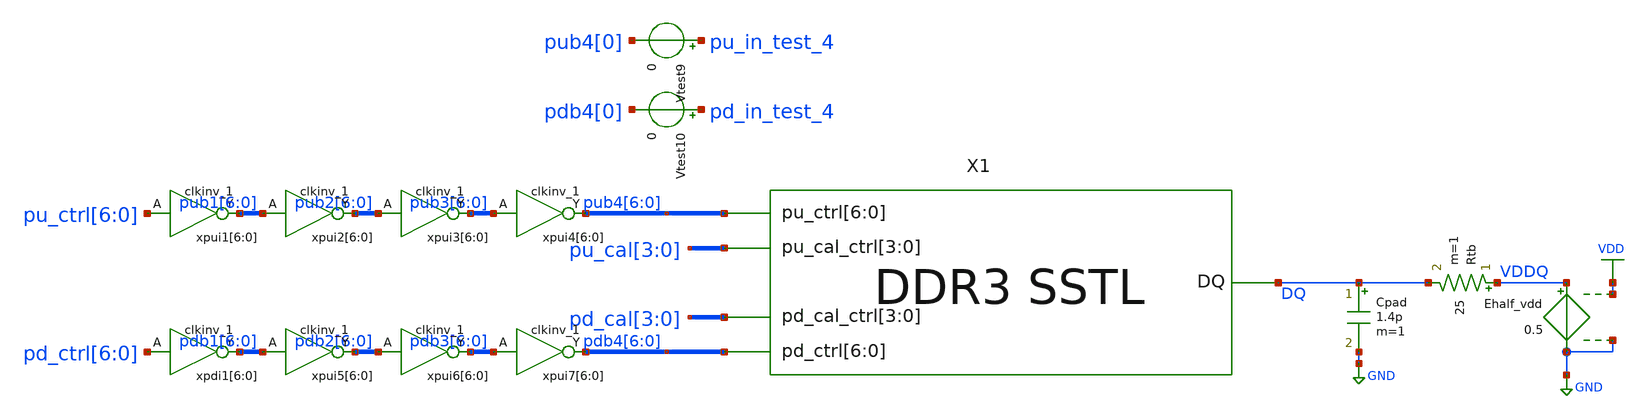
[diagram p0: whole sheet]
** sch_path: schem/sstl_slew_tb.sch
* Copyright 2021 Stefan Frederik Schippers
* Licensed under the Apache License, Version 2.0 (the "License");
* you may not use this file except in compliance with the License.
* You may obtain a copy of the License at
* https://www.apache.org/licenses/LICENSE-2.0
* Unless required by applicable law or agreed to in writing, software
* distributed under the License is distributed on an "AS IS" BASIS,
* WITHOUT WARRANTIES OR CONDITIONS OF ANY KIND, either express or implied.
* See the License for the specific language governing permissions and
* limitations under the License.
**.subckt sstl_slew_tb
X1 DQ pdb4[6] pdb4[5] pdb4[4] pdb4[3] pdb4[2] pdb4[1] pdb4[0] pub4[6] pub4[5] pub4[4] pub4[3]
+ pub4[2] pub4[1] pub4[0] pd_cal[3] pd_cal[2] pd_cal[1] pd_cal[0] pu_cal[3] pu_cal[2] pu_cal[1] pu_cal[0]
+ SSTL
Rtb VDDQ DQ 25 m=1
Cpad DQ GND 1.4p m=1
Ehalf_vdd VDDQ GND VDD GND 0.5
xpui1[6] pu_ctrl[6] GND GND VDD VDD pub1[6] sky130_fd_sc_hd__clkinv_1
xpui1[5] pu_ctrl[5] GND GND VDD VDD pub1[5] sky130_fd_sc_hd__clkinv_1
xpui1[4] pu_ctrl[4] GND GND VDD VDD pub1[4] sky130_fd_sc_hd__clkinv_1
xpui1[3] pu_ctrl[3] GND GND VDD VDD pub1[3] sky130_fd_sc_hd__clkinv_1
xpui1[2] pu_ctrl[2] GND GND VDD VDD pub1[2] sky130_fd_sc_hd__clkinv_1
xpui1[1] pu_ctrl[1] GND GND VDD VDD pub1[1] sky130_fd_sc_hd__clkinv_1
xpui1[0] pu_ctrl[0] GND GND VDD VDD pub1[0] sky130_fd_sc_hd__clkinv_1
xpdi1[6] pd_ctrl[6] VGND VNB VPB VPWR pdb1[6] sky130_fd_sc_hd__clkinv_1
xpdi1[5] pd_ctrl[5] VGND VNB VPB VPWR pdb1[5] sky130_fd_sc_hd__clkinv_1
xpdi1[4] pd_ctrl[4] VGND VNB VPB VPWR pdb1[4] sky130_fd_sc_hd__clkinv_1
xpdi1[3] pd_ctrl[3] VGND VNB VPB VPWR pdb1[3] sky130_fd_sc_hd__clkinv_1
xpdi1[2] pd_ctrl[2] VGND VNB VPB VPWR pdb1[2] sky130_fd_sc_hd__clkinv_1
xpdi1[1] pd_ctrl[1] VGND VNB VPB VPWR pdb1[1] sky130_fd_sc_hd__clkinv_1
xpdi1[0] pd_ctrl[0] VGND VNB VPB VPWR pdb1[0] sky130_fd_sc_hd__clkinv_1
Vtest9 pu_in_test_4 pub4[0] 0
Vtest10 pd_in_test_4 pdb4[0] 0
xpui2[6] pub1[6] GND GND VDD VDD pub2[6] sky130_fd_sc_hd__clkinv_1
xpui2[5] pub1[5] GND GND VDD VDD pub2[5] sky130_fd_sc_hd__clkinv_1
xpui2[4] pub1[4] GND GND VDD VDD pub2[4] sky130_fd_sc_hd__clkinv_1
xpui2[3] pub1[3] GND GND VDD VDD pub2[3] sky130_fd_sc_hd__clkinv_1
xpui2[2] pub1[2] GND GND VDD VDD pub2[2] sky130_fd_sc_hd__clkinv_1
xpui2[1] pub1[1] GND GND VDD VDD pub2[1] sky130_fd_sc_hd__clkinv_1
xpui2[0] pub1[0] GND GND VDD VDD pub2[0] sky130_fd_sc_hd__clkinv_1
xpui3[6] pub2[6] GND GND VDD VDD pub3[6] sky130_fd_sc_hd__clkinv_1
xpui3[5] pub2[5] GND GND VDD VDD pub3[5] sky130_fd_sc_hd__clkinv_1
xpui3[4] pub2[4] GND GND VDD VDD pub3[4] sky130_fd_sc_hd__clkinv_1
xpui3[3] pub2[3] GND GND VDD VDD pub3[3] sky130_fd_sc_hd__clkinv_1
xpui3[2] pub2[2] GND GND VDD VDD pub3[2] sky130_fd_sc_hd__clkinv_1
xpui3[1] pub2[1] GND GND VDD VDD pub3[1] sky130_fd_sc_hd__clkinv_1
xpui3[0] pub2[0] GND GND VDD VDD pub3[0] sky130_fd_sc_hd__clkinv_1
xpui4[6] pub3[6] GND GND VDD VDD pub4[6] sky130_fd_sc_hd__clkinv_1
xpui4[5] pub3[5] GND GND VDD VDD pub4[5] sky130_fd_sc_hd__clkinv_1
xpui4[4] pub3[4] GND GND VDD VDD pub4[4] sky130_fd_sc_hd__clkinv_1
xpui4[3] pub3[3] GND GND VDD VDD pub4[3] sky130_fd_sc_hd__clkinv_1
xpui4[2] pub3[2] GND GND VDD VDD pub4[2] sky130_fd_sc_hd__clkinv_1
xpui4[1] pub3[1] GND GND VDD VDD pub4[1] sky130_fd_sc_hd__clkinv_1
xpui4[0] pub3[0] GND GND VDD VDD pub4[0] sky130_fd_sc_hd__clkinv_1
xpui5[6] pdb1[6] GND GND VDD VDD pdb2[6] sky130_fd_sc_hd__clkinv_1
xpui5[5] pdb1[5] GND GND VDD VDD pdb2[5] sky130_fd_sc_hd__clkinv_1
xpui5[4] pdb1[4] GND GND VDD VDD pdb2[4] sky130_fd_sc_hd__clkinv_1
xpui5[3] pdb1[3] GND GND VDD VDD pdb2[3] sky130_fd_sc_hd__clkinv_1
xpui5[2] pdb1[2] GND GND VDD VDD pdb2[2] sky130_fd_sc_hd__clkinv_1
xpui5[1] pdb1[1] GND GND VDD VDD pdb2[1] sky130_fd_sc_hd__clkinv_1
xpui5[0] pdb1[0] GND GND VDD VDD pdb2[0] sky130_fd_sc_hd__clkinv_1
xpui6[6] pdb2[6] GND GND VDD VDD pdb3[6] sky130_fd_sc_hd__clkinv_1
xpui6[5] pdb2[5] GND GND VDD VDD pdb3[5] sky130_fd_sc_hd__clkinv_1
xpui6[4] pdb2[4] GND GND VDD VDD pdb3[4] sky130_fd_sc_hd__clkinv_1
xpui6[3] pdb2[3] GND GND VDD VDD pdb3[3] sky130_fd_sc_hd__clkinv_1
xpui6[2] pdb2[2] GND GND VDD VDD pdb3[2] sky130_fd_sc_hd__clkinv_1
xpui6[1] pdb2[1] GND GND VDD VDD pdb3[1] sky130_fd_sc_hd__clkinv_1
xpui6[0] pdb2[0] GND GND VDD VDD pdb3[0] sky130_fd_sc_hd__clkinv_1
xpui7[6] pdb3[6] GND GND VDD VDD pdb4[6] sky130_fd_sc_hd__clkinv_1
xpui7[5] pdb3[5] GND GND VDD VDD pdb4[5] sky130_fd_sc_hd__clkinv_1
xpui7[4] pdb3[4] GND GND VDD VDD pdb4[4] sky130_fd_sc_hd__clkinv_1
xpui7[3] pdb3[3] GND GND VDD VDD pdb4[3] sky130_fd_sc_hd__clkinv_1
xpui7[2] pdb3[2] GND GND VDD VDD pdb4[2] sky130_fd_sc_hd__clkinv_1
xpui7[1] pdb3[1] GND GND VDD VDD pdb4[1] sky130_fd_sc_hd__clkinv_1
xpui7[0] pdb3[0] GND GND VDD VDD pdb4[0] sky130_fd_sc_hd__clkinv_1
**** begin user architecture code
 ** Local library links to pdk
.lib ./sky130/libs/SED_process_SED_lib.spice SED_process_SED
.include $::SKYWATER_STDCELLS/sky130_fd_sc_hd.spice

**** end user architecture code
**.ends

* expanding   symbol:  SSTL.sym # of pins=5
** sym_path: schem/SSTL.sym
** sch_path: schem/SSTL.sch
.subckt SSTL DQ pd_ctrl[6] pd_ctrl[5] pd_ctrl[4] pd_ctrl[3] pd_ctrl[2] pd_ctrl[1] pd_ctrl[0]
+ pu_ctrl[6] pu_ctrl[5] pu_ctrl[4] pu_ctrl[3] pu_ctrl[2] pu_ctrl[1] pu_ctrl[0] pd_cal_ctrl[3] pd_cal_ctrl[2]
+ pd_cal_ctrl[1] pd_cal_ctrl[0] pu_cal_ctrl[3] pu_cal_ctrl[2] pu_cal_ctrl[1] pu_cal_ctrl[0]
*.iopin DQ
*.ipin pu_cal_ctrl[3],pu_cal_ctrl[2],pu_cal_ctrl[1],pu_cal_ctrl[0]
*.ipin pd_cal_ctrl[3],pd_cal_ctrl[2],pd_cal_ctrl[1],pd_cal_ctrl[0]
*.ipin pu_ctrl[6],pu_ctrl[5],pu_ctrl[4],pu_ctrl[3],pu_ctrl[2],pu_ctrl[1],pu_ctrl[0]
*.ipin pd_ctrl[6],pd_ctrl[5],pd_ctrl[4],pd_ctrl[3],pd_ctrl[2],pd_ctrl[1],pd_ctrl[0]
X1 DQ n_pu_ctrl[6] n_pu_cal_ctrl[3] n_pu_cal_ctrl[2] n_pu_cal_ctrl[1] n_pu_cal_ctrl[0] p-leg
X2 DQ pd_ctrl_buff[6] pd_cal_ctrl[3] pd_cal_ctrl[2] pd_cal_ctrl[1] pd_cal_ctrl[0] n-leg
X3 DQ n_pu_ctrl[5] n_pu_cal_ctrl[3] n_pu_cal_ctrl[2] n_pu_cal_ctrl[1] n_pu_cal_ctrl[0] p-leg
X4 DQ pd_ctrl_buff[5] pd_cal_ctrl[3] pd_cal_ctrl[2] pd_cal_ctrl[1] pd_cal_ctrl[0] n-leg
X5 DQ n_pu_ctrl[4] n_pu_cal_ctrl[3] n_pu_cal_ctrl[2] n_pu_cal_ctrl[1] n_pu_cal_ctrl[0] p-leg
X6 DQ pd_ctrl_buff[4] pd_cal_ctrl[3] pd_cal_ctrl[2] pd_cal_ctrl[1] pd_cal_ctrl[0] n-leg
X7 DQ n_pu_ctrl[3] n_pu_cal_ctrl[3] n_pu_cal_ctrl[2] n_pu_cal_ctrl[1] n_pu_cal_ctrl[0] p-leg
X8 DQ pd_ctrl_buff[3] pd_cal_ctrl[3] pd_cal_ctrl[2] pd_cal_ctrl[1] pd_cal_ctrl[0] n-leg
X9 DQ n_pu_ctrl[2] n_pu_cal_ctrl[3] n_pu_cal_ctrl[2] n_pu_cal_ctrl[1] n_pu_cal_ctrl[0] p-leg
X10 DQ pd_ctrl_buff[2] pd_cal_ctrl[3] pd_cal_ctrl[2] pd_cal_ctrl[1] pd_cal_ctrl[0] n-leg
X11 DQ n_pu_ctrl[1] n_pu_cal_ctrl[3] n_pu_cal_ctrl[2] n_pu_cal_ctrl[1] n_pu_cal_ctrl[0] p-leg
X12 DQ pd_ctrl_buff[1] pd_cal_ctrl[3] pd_cal_ctrl[2] pd_cal_ctrl[1] pd_cal_ctrl[0] n-leg
X13 DQ n_pu_ctrl[0] n_pu_cal_ctrl[3] n_pu_cal_ctrl[2] n_pu_cal_ctrl[1] n_pu_cal_ctrl[0] p-leg
X14 DQ pd_ctrl_buff[0] pd_cal_ctrl[3] pd_cal_ctrl[2] pd_cal_ctrl[1] pd_cal_ctrl[0] n-leg
xpd_buff_4[6] pdc2[6] VGND VNB VPB VPWR pdc4[6] sky130_fd_sc_hd__clkinv_4
xpd_buff_4[5] pdc2[5] VGND VNB VPB VPWR pdc4[5] sky130_fd_sc_hd__clkinv_4
xpd_buff_4[4] pdc2[4] VGND VNB VPB VPWR pdc4[4] sky130_fd_sc_hd__clkinv_4
xpd_buff_4[3] pdc2[3] VGND VNB VPB VPWR pdc4[3] sky130_fd_sc_hd__clkinv_4
xpd_buff_4[2] pdc2[2] VGND VNB VPB VPWR pdc4[2] sky130_fd_sc_hd__clkinv_4
xpd_buff_4[1] pdc2[1] VGND VNB VPB VPWR pdc4[1] sky130_fd_sc_hd__clkinv_4
xpd_buff_4[0] pdc2[0] VGND VNB VPB VPWR pdc4[0] sky130_fd_sc_hd__clkinv_4
xpd_buff_6[6] pdc4[6] VGND VNB VPB VPWR pd_ctrl_buff[6] sky130_fd_sc_hd__clkbuf_8
xpd_buff_6[5] pdc4[5] VGND VNB VPB VPWR pd_ctrl_buff[5] sky130_fd_sc_hd__clkbuf_8
xpd_buff_6[4] pdc4[4] VGND VNB VPB VPWR pd_ctrl_buff[4] sky130_fd_sc_hd__clkbuf_8
xpd_buff_6[3] pdc4[3] VGND VNB VPB VPWR pd_ctrl_buff[3] sky130_fd_sc_hd__clkbuf_8
xpd_buff_6[2] pdc4[2] VGND VNB VPB VPWR pd_ctrl_buff[2] sky130_fd_sc_hd__clkbuf_8
xpd_buff_6[1] pdc4[1] VGND VNB VPB VPWR pd_ctrl_buff[1] sky130_fd_sc_hd__clkbuf_8
xpd_buff_6[0] pdc4[0] VGND VNB VPB VPWR pd_ctrl_buff[0] sky130_fd_sc_hd__clkbuf_8
xpu_buff_4[6] pu_ctrl[6] VGND VNB VPB VPWR puc4[6] sky130_fd_sc_hd__clkbuf_16
xpu_buff_4[5] pu_ctrl[5] VGND VNB VPB VPWR puc4[5] sky130_fd_sc_hd__clkbuf_16
xpu_buff_4[4] pu_ctrl[4] VGND VNB VPB VPWR puc4[4] sky130_fd_sc_hd__clkbuf_16
xpu_buff_4[3] pu_ctrl[3] VGND VNB VPB VPWR puc4[3] sky130_fd_sc_hd__clkbuf_16
xpu_buff_4[2] pu_ctrl[2] VGND VNB VPB VPWR puc4[2] sky130_fd_sc_hd__clkbuf_16
xpu_buff_4[1] pu_ctrl[1] VGND VNB VPB VPWR puc4[1] sky130_fd_sc_hd__clkbuf_16
xpu_buff_4[0] pu_ctrl[0] VGND VNB VPB VPWR puc4[0] sky130_fd_sc_hd__clkbuf_16
xpu_buff_6[6] puc4[6] VGND VNB VPB VPWR n_pu_ctrl[6] sky130_fd_sc_hd__clkinv_16
xpu_buff_6[5] puc4[5] VGND VNB VPB VPWR n_pu_ctrl[5] sky130_fd_sc_hd__clkinv_16
xpu_buff_6[4] puc4[4] VGND VNB VPB VPWR n_pu_ctrl[4] sky130_fd_sc_hd__clkinv_16
xpu_buff_6[3] puc4[3] VGND VNB VPB VPWR n_pu_ctrl[3] sky130_fd_sc_hd__clkinv_16
xpu_buff_6[2] puc4[2] VGND VNB VPB VPWR n_pu_ctrl[2] sky130_fd_sc_hd__clkinv_16
xpu_buff_6[1] puc4[1] VGND VNB VPB VPWR n_pu_ctrl[1] sky130_fd_sc_hd__clkinv_16
xpu_buff_6[0] puc4[0] VGND VNB VPB VPWR n_pu_ctrl[0] sky130_fd_sc_hd__clkinv_16
xpu_cal_inv[3] pu_cal_ctrl[3] VGND VNB VPB VPWR n_pu_cal_ctrl[3] sky130_fd_sc_hd__inv_1
xpu_cal_inv[2] pu_cal_ctrl[2] VGND VNB VPB VPWR n_pu_cal_ctrl[2] sky130_fd_sc_hd__inv_1
xpu_cal_inv[1] pu_cal_ctrl[1] VGND VNB VPB VPWR n_pu_cal_ctrl[1] sky130_fd_sc_hd__inv_1
xpu_cal_inv[0] pu_cal_ctrl[0] VGND VNB VPB VPWR n_pu_cal_ctrl[0] sky130_fd_sc_hd__inv_1
V1 VDD VPWR 0
V2 VGND GND 0
V3 VDD VPB 0
V4 VNB GND 0
Vpd_ctrl_0 v_pd_ctrl_0 pd_ctrl_buff[6] 0
Vpd_ctrl_1 v_pu_ctrl_0 n_pu_ctrl[6] 0
xpu_buff_2[6] puc4[6] VGND VNB VPB VPWR n_pu_ctrl[6] sky130_fd_sc_hd__clkinv_16
xpu_buff_2[5] puc4[5] VGND VNB VPB VPWR n_pu_ctrl[5] sky130_fd_sc_hd__clkinv_16
xpu_buff_2[4] puc4[4] VGND VNB VPB VPWR n_pu_ctrl[4] sky130_fd_sc_hd__clkinv_16
xpu_buff_2[3] puc4[3] VGND VNB VPB VPWR n_pu_ctrl[3] sky130_fd_sc_hd__clkinv_16
xpu_buff_2[2] puc4[2] VGND VNB VPB VPWR n_pu_ctrl[2] sky130_fd_sc_hd__clkinv_16
xpu_buff_2[1] puc4[1] VGND VNB VPB VPWR n_pu_ctrl[1] sky130_fd_sc_hd__clkinv_16
xpu_buff_2[0] puc4[0] VGND VNB VPB VPWR n_pu_ctrl[0] sky130_fd_sc_hd__clkinv_16
xpd_buff_1[6] pd_ctrl[6] VGND VNB VPB VPWR pdc2[6] sky130_fd_sc_hd__clkinv_4
xpd_buff_1[5] pd_ctrl[5] VGND VNB VPB VPWR pdc2[5] sky130_fd_sc_hd__clkinv_4
xpd_buff_1[4] pd_ctrl[4] VGND VNB VPB VPWR pdc2[4] sky130_fd_sc_hd__clkinv_4
xpd_buff_1[3] pd_ctrl[3] VGND VNB VPB VPWR pdc2[3] sky130_fd_sc_hd__clkinv_4
xpd_buff_1[2] pd_ctrl[2] VGND VNB VPB VPWR pdc2[2] sky130_fd_sc_hd__clkinv_4
xpd_buff_1[1] pd_ctrl[1] VGND VNB VPB VPWR pdc2[1] sky130_fd_sc_hd__clkinv_4
xpd_buff_1[0] pd_ctrl[0] VGND VNB VPB VPWR pdc2[0] sky130_fd_sc_hd__clkinv_4
xpu_buff_1[6] puc4[6] VGND VNB VPB VPWR n_pu_ctrl[6] sky130_fd_sc_hd__clkinv_16
xpu_buff_1[5] puc4[5] VGND VNB VPB VPWR n_pu_ctrl[5] sky130_fd_sc_hd__clkinv_16
xpu_buff_1[4] puc4[4] VGND VNB VPB VPWR n_pu_ctrl[4] sky130_fd_sc_hd__clkinv_16
xpu_buff_1[3] puc4[3] VGND VNB VPB VPWR n_pu_ctrl[3] sky130_fd_sc_hd__clkinv_16
xpu_buff_1[2] puc4[2] VGND VNB VPB VPWR n_pu_ctrl[2] sky130_fd_sc_hd__clkinv_16
xpu_buff_1[1] puc4[1] VGND VNB VPB VPWR n_pu_ctrl[1] sky130_fd_sc_hd__clkinv_16
xpu_buff_1[0] puc4[0] VGND VNB VPB VPWR n_pu_ctrl[0] sky130_fd_sc_hd__clkinv_16
.ends


* expanding   symbol:  p-leg.sym # of pins=3
** sym_path: schem/p-leg.sym
** sch_path: schem/p-leg.sch
.subckt p-leg DQ n_pu_ctrl n_cal_ctrl[3] n_cal_ctrl[2] n_cal_ctrl[1] n_cal_ctrl[0]
*.ipin n_cal_ctrl[3],n_cal_ctrl[2],n_cal_ctrl[1],n_cal_ctrl[0]
*.ipin n_pu_ctrl
*.iopin DQ
XR1 DQ net1 sky130_fd_pr__res_generic_po W=0.33 L=1.8 m=1
XMpullup net1 n_pu_ctrl VDD VDD sky130_fd_pr__pfet_01v8_lvt L=0.35 W=1 nf=1 ad='int((nf+1)/2) * W/nf * 0.29'
+ as='int((nf+2)/2) * W/nf * 0.29' pd='2*int((nf+1)/2) * (W/nf + 0.29)' ps='2*int((nf+2)/2) * (W/nf + 0.29)'
+ nrd='0.29 / W' nrs='0.29 / W' sa=0 sb=0 sd=0 mult=128 m=128
XMctrltot VDD n_cal_ctrl[0] VDD VDD sky130_fd_pr__pfet_01v8_lvt L=0.35 W=1 nf=1 ad='int((nf+1)/2) * W/nf * 0.29'
+ as='int((nf+2)/2) * W/nf * 0.29' pd='2*int((nf+1)/2) * (W/nf + 0.29)' ps='2*int((nf+2)/2) * (W/nf + 0.29)'
+ nrd='0.29 / W' nrs='0.29 / W' sa=0 sb=0 sd=0 mult=120 m=120
XMctrl0 DQ n_cal_ctrl[0] net1 VDD sky130_fd_pr__pfet_01v8_lvt L=0.35 W=1 nf=1 ad='int((nf+1)/2) * W/nf * 0.29'
+ as='int((nf+2)/2) * W/nf * 0.29' pd='2*int((nf+1)/2) * (W/nf + 0.29)' ps='2*int((nf+2)/2) * (W/nf + 0.29)'
+ nrd='0.29 / W' nrs='0.29 / W' sa=0 sb=0 sd=0 mult=48 m=48
XMctrl1 DQ n_cal_ctrl[1] net1 VDD sky130_fd_pr__pfet_01v8_lvt L=0.35 W=1 nf=1 ad='int((nf+1)/2) * W/nf * 0.29'
+ as='int((nf+2)/2) * W/nf * 0.29' pd='2*int((nf+1)/2) * (W/nf + 0.29)' ps='2*int((nf+2)/2) * (W/nf + 0.29)'
+ nrd='0.29 / W' nrs='0.29 / W' sa=0 sb=0 sd=0 mult=16 m=16
XMctrl2 DQ n_cal_ctrl[2] net1 VDD sky130_fd_pr__pfet_01v8_lvt L=0.35 W=1 nf=1 ad='int((nf+1)/2) * W/nf * 0.29'
+ as='int((nf+2)/2) * W/nf * 0.29' pd='2*int((nf+1)/2) * (W/nf + 0.29)' ps='2*int((nf+2)/2) * (W/nf + 0.29)'
+ nrd='0.29 / W' nrs='0.29 / W' sa=0 sb=0 sd=0 mult=8 m=8
XMctrl3 DQ n_cal_ctrl[3] net1 VDD sky130_fd_pr__pfet_01v8_lvt L=0.35 W=1 nf=1 ad='int((nf+1)/2) * W/nf * 0.29'
+ as='int((nf+2)/2) * W/nf * 0.29' pd='2*int((nf+1)/2) * (W/nf + 0.29)' ps='2*int((nf+2)/2) * (W/nf + 0.29)'
+ nrd='0.29 / W' nrs='0.29 / W' sa=0 sb=0 sd=0 mult=4 m=4
.ends


* expanding   symbol:  n-leg.sym # of pins=3
** sym_path: schem/n-leg.sym
** sch_path: schem/n-leg.sch
.subckt n-leg DQ pd_ctrl cal_ctrl[3] cal_ctrl[2] cal_ctrl[1] cal_ctrl[0]
*.iopin DQ
*.ipin pd_ctrl
*.ipin cal_ctrl[3],cal_ctrl[2],cal_ctrl[1],cal_ctrl[0]
XR1 vpulldown DQ sky130_fd_pr__res_generic_po W=0.33 L=1.7 m=1
Xn1 vpulldown pd_ctrl GND GND sky130_fd_pr__nfet_01v8 L=0.15 W=0.65 nf=1 ad='int((nf+1)/2) * W/nf * 0.29'
+ as='int((nf+2)/2) * W/nf * 0.29' pd='2*int((nf+1)/2) * (W/nf + 0.29)' ps='2*int((nf+2)/2) * (W/nf + 0.29)'
+ nrd='0.29 / W' nrs='0.29 / W' sa=0 sb=0 sd=0 mult=48 m=48
Xnctrl0 DQ cal_ctrl[0] vpulldown GND sky130_fd_pr__nfet_01v8 L=0.15 W=0.65 nf=1 ad='int((nf+1)/2) * W/nf * 0.29'
+ as='int((nf+2)/2) * W/nf * 0.29' pd='2*int((nf+1)/2) * (W/nf + 0.29)' ps='2*int((nf+2)/2) * (W/nf + 0.29)'
+ nrd='0.29 / W' nrs='0.29 / W' sa=0 sb=0 sd=0 mult=6 m=6
Xnctrl1 DQ cal_ctrl[1] vpulldown GND sky130_fd_pr__nfet_01v8 L=0.15 W=0.65 nf=1 ad='int((nf+1)/2) * W/nf * 0.29'
+ as='int((nf+2)/2) * W/nf * 0.29' pd='2*int((nf+1)/2) * (W/nf + 0.29)' ps='2*int((nf+2)/2) * (W/nf + 0.29)'
+ nrd='0.29 / W' nrs='0.29 / W' sa=0 sb=0 sd=0 mult=3 m=3
Xnctrl2 DQ cal_ctrl[2] vpulldown GND sky130_fd_pr__nfet_01v8 L=0.15 W=0.975 nf=1 ad='int((nf+1)/2) * W/nf * 0.29'
+ as='int((nf+2)/2) * W/nf * 0.29' pd='2*int((nf+1)/2) * (W/nf + 0.29)' ps='2*int((nf+2)/2) * (W/nf + 0.29)'
+ nrd='0.29 / W' nrs='0.29 / W' sa=0 sb=0 sd=0 mult=1 m=1
Xnctrl3 DQ cal_ctrl[3] vpulldown GND sky130_fd_pr__nfet_01v8 L=0.15 W=0.5 nf=1 ad='int((nf+1)/2) * W/nf * 0.29'
+ as='int((nf+2)/2) * W/nf * 0.29' pd='2*int((nf+1)/2) * (W/nf + 0.29)' ps='2*int((nf+2)/2) * (W/nf + 0.29)'
+ nrd='0.29 / W' nrs='0.29 / W' sa=0 sb=0 sd=0 mult=1 m=1
Xnctrl_tot GND GND GND GND sky130_fd_pr__nfet_01v8 L=0.15 W=0.65 nf=1 ad='int((nf+1)/2) * W/nf * 0.29'
+ as='int((nf+2)/2) * W/nf * 0.29' pd='2*int((nf+1)/2) * (W/nf + 0.29)' ps='2*int((nf+2)/2) * (W/nf + 0.29)'
+ nrd='0.29 / W' nrs='0.29 / W' sa=0 sb=0 sd=0 mult=11 m=11
.ends

.GLOBAL GND
.GLOBAL VDD
**** begin user architecture code


* power voltage
vvdd VDD 0 SED_vdd_SED

** CALIBRATION CONTROL **
* PULLUP
vpu_cal0 pu_cal[0] 0 SED_pucal0_SED
vpu_cal1 pu_cal[1] 0 SED_pucal1_SED
vpu_cal2 pu_cal[2] 0 SED_pucal2_SED
vpu_cal3 pu_cal[3] 0 SED_pucal3_SED
* PULLDOWN
vpd_cal0 pd_cal[0] 0 SED_pdcal0_SED
vpd_cal1 pd_cal[1] 0 SED_pdcal1_SED
vpd_cal2 pd_cal[2] 0 SED_pdcal2_SED
vpd_cal3 pd_cal[3] 0 SED_pdcal3_SED

** LEG ENABLE/DISABLE CONTROL
* PULLUP
*          vlow, vhigh, delay, risetime, falltime, pulsewidth, period, phase
vpu_ctrl0 pu_ctrl[0] 0 0 PULSE 0   SED_puctrl0_SED 1n 10p 10p 5n 10n 0
vpu_ctrl1 pu_ctrl[1] 0 0 PULSE 0   SED_puctrl1_SED 1n 10p 10p 5n 10n 0
vpu_ctrl2 pu_ctrl[2] 0 0 PULSE 0   SED_puctrl2_SED 1n 10p 10p 5n 10n 0
vpu_ctrl3 pu_ctrl[3] 0 0 PULSE 0   SED_puctrl3_SED 1n 10p 10p 5n 10n 0
vpu_ctrl4 pu_ctrl[4] 0 0 PULSE 0   SED_puctrl4_SED 1n 10p 10p 5n 10n 0
vpu_ctrl5 pu_ctrl[5] 0 0 PULSE 0   SED_puctrl5_SED 1n 10p 10p 5n 10n 0
vpu_ctrl6 pu_ctrl[6] 0 0 PULSE 0   SED_puctrl6_SED 1n 10p 10p 5n 10n 0
* PULLDOWN (delay was set to 1.1n for better slew...)
vpd_ctrl0 VDD pd_ctrl[0] 0 PULSE 0 SED_pdctrl0_SED 1n 10p 10p 5n 10n 0
vpd_ctrl1 VDD pd_ctrl[1] 0 PULSE 0 SED_pdctrl1_SED 1n 10p 10p 5n 10n 0
vpd_ctrl2 VDD pd_ctrl[2] 0 PULSE 0 SED_pdctrl2_SED 1n 10p 10p 5n 10n 0
vpd_ctrl3 VDD pd_ctrl[3] 0 PULSE 0 SED_pdctrl3_SED 1n 10p 10p 5n 10n 0
vpd_ctrl4 VDD pd_ctrl[4] 0 PULSE 0 SED_pdctrl4_SED 1n 10p 10p 5n 10n 0
vpd_ctrl5 VDD pd_ctrl[5] 0 PULSE 0 SED_pdctrl5_SED 1n 10p 10p 5n 10n 0
vpd_ctrl6 VDD pd_ctrl[6] 0 PULSE 0 SED_pdctrl6_SED 1n 10p 10p 5n 10n 0

.control
save all
set temp=SED_temp_SED

* RUN SIMULATION
tran 1p 8n
* Measure rise time
meas tran tdiff_rise trig dq val=SED_volac_SED rise=1 targ dq val=SED_vohac_SED rise=1
* Measure fall time
meas tran tdiff_fall trig dq val=SED_vohac_SED fall=1 targ dq val=SED_volac_SED fall=1

* OUTPUT
wrdata ./out/SED_plotName_SED/SED_plotName_SED.txt tdiff_rise tdiff_fall
set hcopydevtype = svg
hardcopy ./out/SED_plotName_SED/SED_plotName_SED.svg dq pu_in_test_4 pd_in_test_4 title 'DQ vs time'

*plot dq pu_in_test_4 pd_in_test_4 x1.v_pu_ctrl_0 x1.v_pd_ctrl_0

.endc


**** end user architecture code
.end
